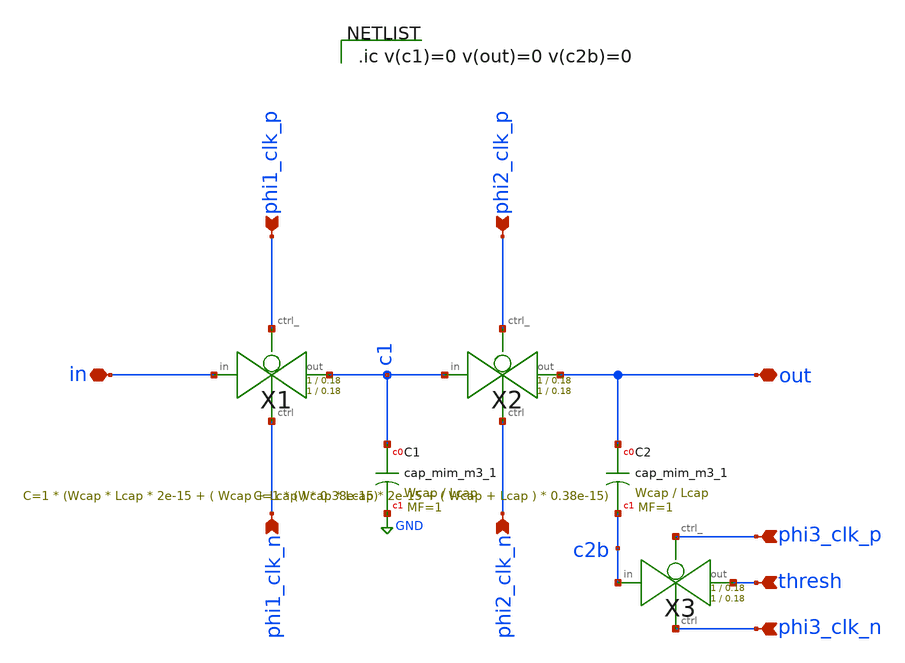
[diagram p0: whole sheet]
** sch_path: xschem/Switched_Caps/2switchcaps_thresh.sch
**.subckt 2switchcaps_thresh out in phi1_clk_n phi1_clk_p phi2_clk_p phi2_clk_n thresh phi3_clk_n
*+ phi3_clk_p
*.iopin out
*.iopin in
*.ipin phi1_clk_n
*.ipin phi1_clk_p
*.ipin phi2_clk_p
*.ipin phi2_clk_n
*.ipin thresh
*.ipin phi3_clk_n
*.ipin phi3_clk_p
XC1 c1 GND sky130_fd_pr__cap_mim_m3_1 W=Wcap L=Lcap MF=1 m=1
X1 in c1 phi1_clk_p phi1_clk_n transmission_gate Wpmos=1 Lpmos=0.18 Wnmos=1 Lnmos=0.18
X2 c1 out phi2_clk_p phi2_clk_n transmission_gate Wpmos=1 Lpmos=0.18 Wnmos=1 Lnmos=0.18
XC2 out c2b sky130_fd_pr__cap_mim_m3_1 W=Wcap L=Lcap MF=1 m=1
X3 c2b thresh phi3_clk_p phi3_clk_n transmission_gate Wpmos=1 Lpmos=0.18 Wnmos=1 Lnmos=0.18
**** begin user architecture code

.ic v(c1)=0 v(out)=0 v(c2b)=0

**** end user architecture code
**.ends

* expanding   symbol:  transmission_gate/transmission_gate.sym # of pins=4
** sym_path: xschem/transmission_gate/transmission_gate.sym
** sch_path: xschem/transmission_gate/transmission_gate.sch
.subckt transmission_gate in out ctrl_ ctrl  Wpmos=1 Lpmos=0.18 Wnmos=1 Lnmos=0.18
*.iopin in
*.iopin out
*.ipin ctrl_
*.ipin ctrl
XM1 in ctrl out GND sky130_fd_pr__nfet_01v8 L=Lnmos W=Wnmos nf=1 ad='int((nf+1)/2) * W/nf * 0.29' as='int((nf+2)/2) * W/nf * 0.29'
+ pd='2*int((nf+1)/2) * (W/nf + 0.29)' ps='2*int((nf+2)/2) * (W/nf + 0.29)' nrd='0.29 / W' nrs='0.29 / W'
+ sa=0 sb=0 sd=0 mult=1 m=1
XM2 out ctrl_ in VDD sky130_fd_pr__pfet_01v8 L=Lpmos W=Wpmos nf=1 ad='int((nf+1)/2) * W/nf * 0.29' as='int((nf+2)/2) * W/nf * 0.29'
+ pd='2*int((nf+1)/2) * (W/nf + 0.29)' ps='2*int((nf+2)/2) * (W/nf + 0.29)' nrd='0.29 / W' nrs='0.29 / W'
+ sa=0 sb=0 sd=0 mult=1 m=1
.ends

.GLOBAL GND
.GLOBAL VDD
.end
